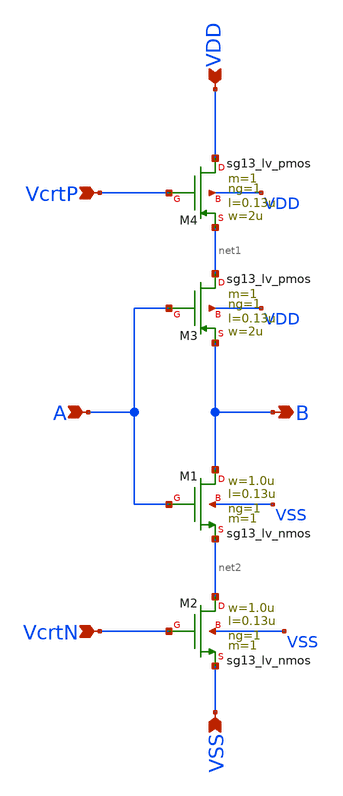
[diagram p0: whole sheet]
** sch_path: work/integrator_curstav_inv/xschem/integrator_curstav_inv.sch
**.subckt integrator_curstav_inv VDD VSS A B VcrtP VcrtN
*.ipin VDD
*.ipin VSS
*.ipin A
*.opin B
*.ipin VcrtP
*.ipin VcrtN
XM1 B A net2 VSS sg13_lv_nmos w=1.0u l=0.13u ng=1 m=1 mm_ok=1
XM2 net2 VcrtN VSS VSS sg13_lv_nmos w=1.0u l=0.13u ng=1 m=1 mm_ok=1
XM3 net1 A B VDD sg13_lv_pmos w=2u l=0.13u ng=1 m=1 mm_ok=1
XM4 VDD VcrtP net1 VDD sg13_lv_pmos w=2u l=0.13u ng=1 m=1 mm_ok=1
**.ends
.end
